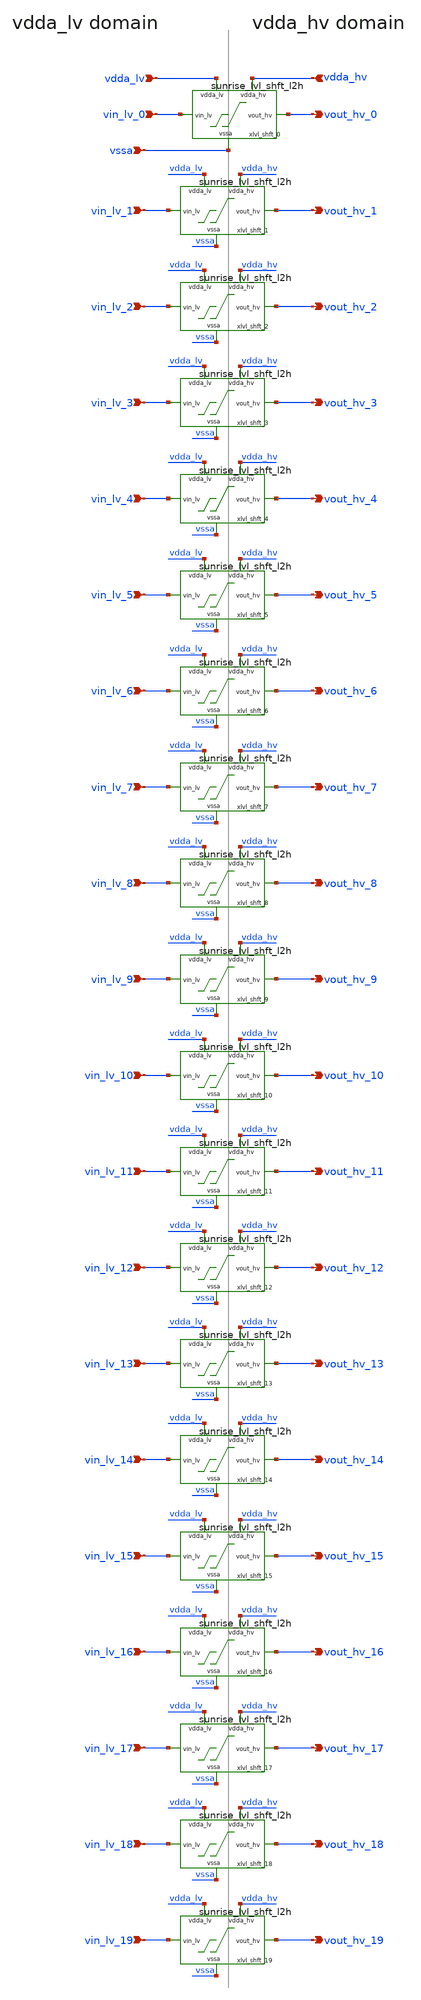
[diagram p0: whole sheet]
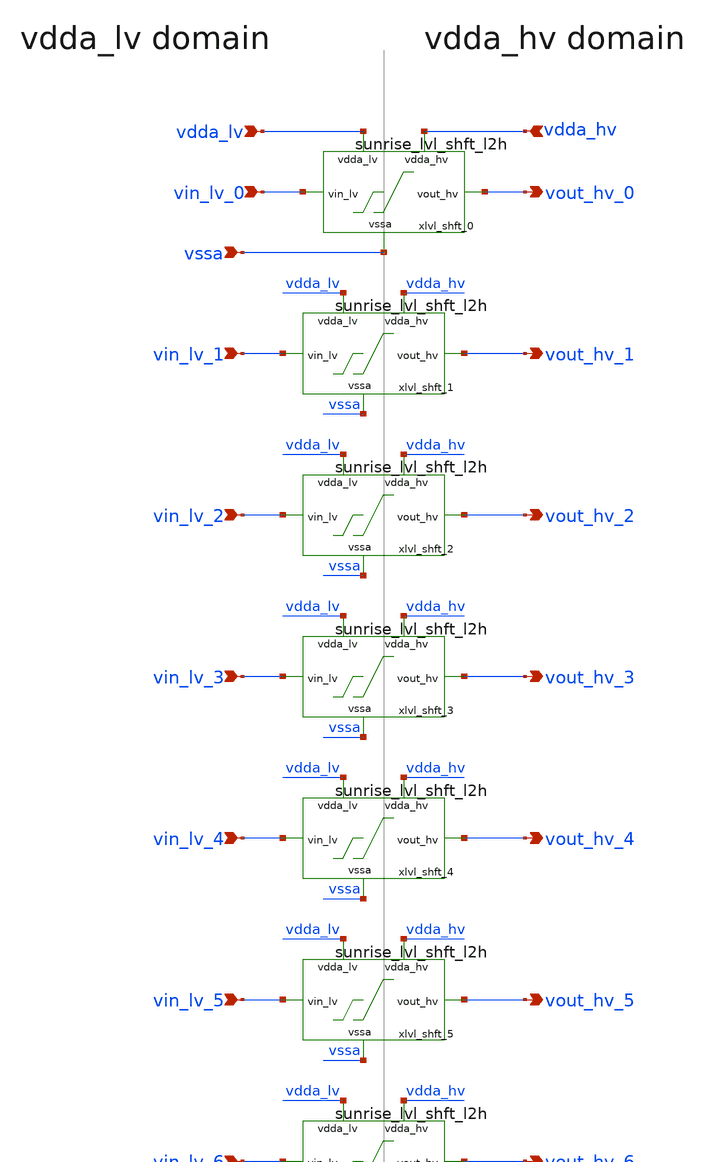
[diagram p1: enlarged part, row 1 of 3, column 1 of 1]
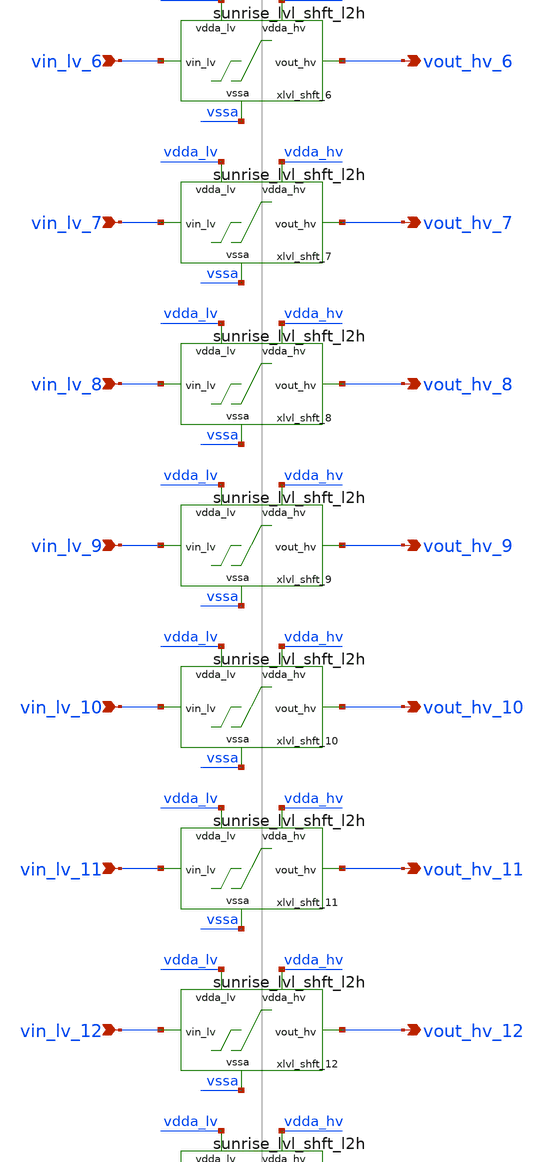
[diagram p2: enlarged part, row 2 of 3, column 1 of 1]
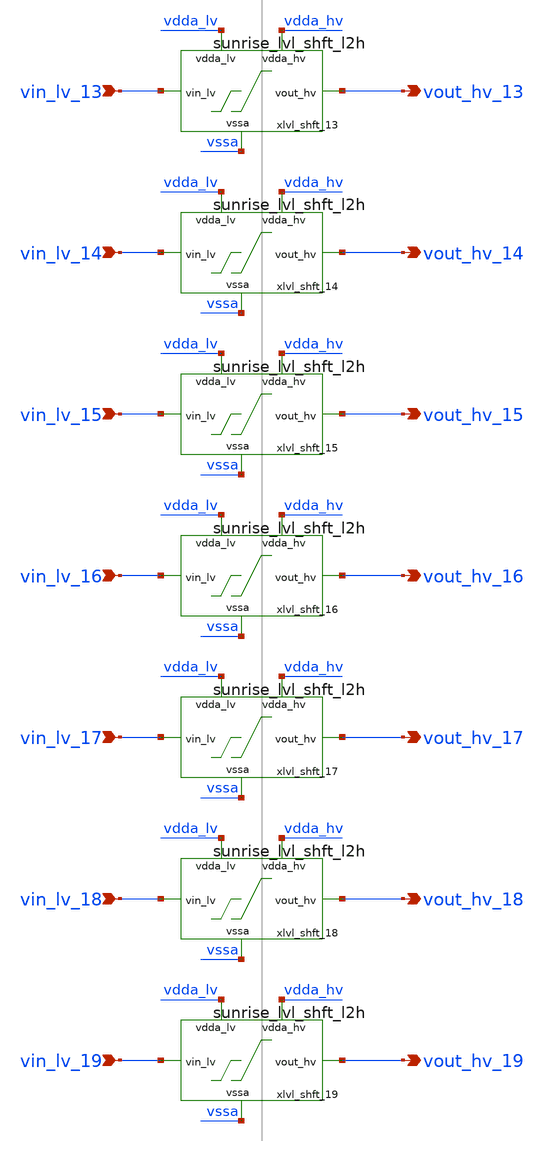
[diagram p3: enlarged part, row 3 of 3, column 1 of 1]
** sch_path: Schematics_Layout/sunrise_lvl_shft/sunrise_lvl_shft.sch
**.subckt sunrise_lvl_shft vin_lv_0 vout_hv_0 vin_lv_1 vout_hv_1 vin_lv_2 vout_hv_2 vin_lv_3
*+ vout_hv_3 vin_lv_4 vout_hv_4 vin_lv_5 vout_hv_5 vin_lv_6 vout_hv_6 vin_lv_7 vout_hv_7 vin_lv_8 vout_hv_8
*+ vin_lv_9 vout_hv_9 vin_lv_10 vout_hv_10 vin_lv_11 vout_hv_11 vin_lv_12 vout_hv_12 vin_lv_13 vout_hv_13
*+ vin_lv_14 vout_hv_14 vin_lv_15 vout_hv_15 vin_lv_16 vout_hv_16 vin_lv_17 vout_hv_17 vin_lv_18 vout_hv_18
*+ vin_lv_19 vout_hv_19 vdda_lv vssa vdda_hv
*.ipin vin_lv_0
*.opin vout_hv_0
*.ipin vin_lv_1
*.opin vout_hv_1
*.ipin vin_lv_2
*.opin vout_hv_2
*.ipin vin_lv_3
*.opin vout_hv_3
*.ipin vin_lv_4
*.opin vout_hv_4
*.ipin vin_lv_5
*.opin vout_hv_5
*.ipin vin_lv_6
*.opin vout_hv_6
*.ipin vin_lv_7
*.opin vout_hv_7
*.ipin vin_lv_8
*.opin vout_hv_8
*.ipin vin_lv_9
*.opin vout_hv_9
*.ipin vin_lv_10
*.opin vout_hv_10
*.ipin vin_lv_11
*.opin vout_hv_11
*.ipin vin_lv_12
*.opin vout_hv_12
*.ipin vin_lv_13
*.opin vout_hv_13
*.ipin vin_lv_14
*.opin vout_hv_14
*.ipin vin_lv_15
*.opin vout_hv_15
*.ipin vin_lv_16
*.opin vout_hv_16
*.ipin vin_lv_17
*.opin vout_hv_17
*.ipin vin_lv_18
*.opin vout_hv_18
*.ipin vin_lv_19
*.opin vout_hv_19
*.ipin vdda_lv
*.ipin vssa
*.ipin vdda_hv
xlvl_shft_0 vdda_hv vout_hv_0 vdda_lv vin_lv_0 vssa sunrise_lvl_shft_l2h
xlvl_shft_1 vdda_hv vout_hv_1 vdda_lv vin_lv_1 vssa sunrise_lvl_shft_l2h
xlvl_shft_2 vdda_hv vout_hv_2 vdda_lv vin_lv_2 vssa sunrise_lvl_shft_l2h
xlvl_shft_3 vdda_hv vout_hv_3 vdda_lv vin_lv_3 vssa sunrise_lvl_shft_l2h
xlvl_shft_4 vdda_hv vout_hv_4 vdda_lv vin_lv_4 vssa sunrise_lvl_shft_l2h
xlvl_shft_5 vdda_hv vout_hv_5 vdda_lv vin_lv_5 vssa sunrise_lvl_shft_l2h
xlvl_shft_6 vdda_hv vout_hv_6 vdda_lv vin_lv_6 vssa sunrise_lvl_shft_l2h
xlvl_shft_7 vdda_hv vout_hv_7 vdda_lv vin_lv_7 vssa sunrise_lvl_shft_l2h
xlvl_shft_8 vdda_hv vout_hv_8 vdda_lv vin_lv_8 vssa sunrise_lvl_shft_l2h
xlvl_shft_9 vdda_hv vout_hv_9 vdda_lv vin_lv_9 vssa sunrise_lvl_shft_l2h
xlvl_shft_10 vdda_hv vout_hv_10 vdda_lv vin_lv_10 vssa sunrise_lvl_shft_l2h
xlvl_shft_11 vdda_hv vout_hv_11 vdda_lv vin_lv_11 vssa sunrise_lvl_shft_l2h
xlvl_shft_12 vdda_hv vout_hv_12 vdda_lv vin_lv_12 vssa sunrise_lvl_shft_l2h
xlvl_shft_13 vdda_hv vout_hv_13 vdda_lv vin_lv_13 vssa sunrise_lvl_shft_l2h
xlvl_shft_14 vdda_hv vout_hv_14 vdda_lv vin_lv_14 vssa sunrise_lvl_shft_l2h
xlvl_shft_15 vdda_hv vout_hv_15 vdda_lv vin_lv_15 vssa sunrise_lvl_shft_l2h
xlvl_shft_16 vdda_hv vout_hv_16 vdda_lv vin_lv_16 vssa sunrise_lvl_shft_l2h
xlvl_shft_17 vdda_hv vout_hv_17 vdda_lv vin_lv_17 vssa sunrise_lvl_shft_l2h
xlvl_shft_18 vdda_hv vout_hv_18 vdda_lv vin_lv_18 vssa sunrise_lvl_shft_l2h
xlvl_shft_19 vdda_hv vout_hv_19 vdda_lv vin_lv_19 vssa sunrise_lvl_shft_l2h
**.ends

* expanding   symbol:  sunrise_lvl_shft_l2h.sym # of pins=5
** sym_path: Schematics_Layout/sunrise_lvl_shft_l2h/sunrise_lvl_shft_l2h.sym
** sch_path: Schematics_Layout/sunrise_lvl_shft_l2h/sunrise_lvl_shft_l2h.sch
.subckt sunrise_lvl_shft_l2h vdda_hv vout_hv vdda_lv vin_lv vssa
*.ipin vdda_hv
*.ipin vdda_lv
*.ipin vssa
*.ipin vin_lv
*.opin vout_hv
XM1 lvlsh in_b vssa vssa sg13_hv_nmos w=2u l=0.45u ng=1 m=1 mm_ok=1
XM2 lvlsh_b vin_lv vssa vssa sg13_hv_nmos w=2u l=0.45u ng=1 m=1 mm_ok=1
XM3 lvlsh lvlsh_b vdda_hv vdda_hv sg13_hv_pmos w=0.3u l=0.45u ng=1 m=1 mm_ok=1
XM4 lvlsh_b lvlsh vdda_hv vdda_hv sg13_hv_pmos w=0.3u l=0.45u ng=1 m=1 mm_ok=1
XM7 vout_hv lvlsh_b vssa vssa sg13_hv_nmos w=2u l=0.45u ng=1 m=1 mm_ok=1
XM8 vout_hv lvlsh_b vdda_hv vdda_hv sg13_hv_pmos w=2u l=0.4u ng=1 m=2 mm_ok=1
x1 in_b vin_lv vdda_lv vssa sg13cmos5l_inv_2
* noconn vdda_lv
.ends

.end
